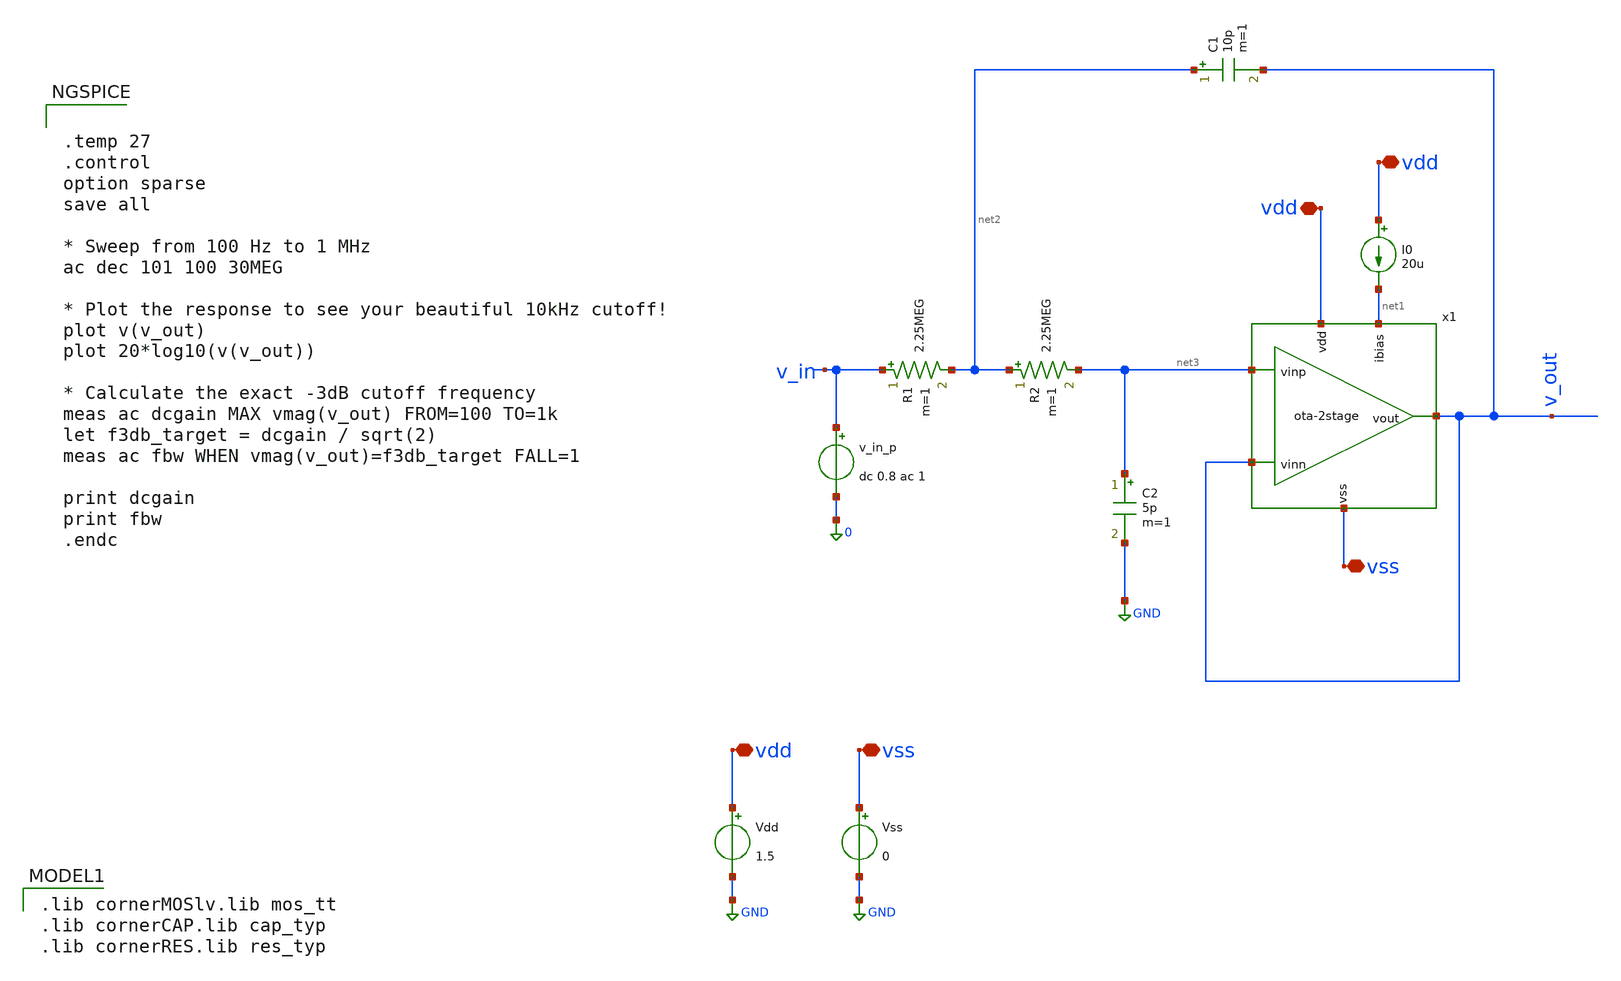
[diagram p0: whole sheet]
** sch_path: Testbench/ota-2stage_tb-sk-lpf.sch
**.subckt ota-2stage_tb-sk-lpf vdd vdd vdd vss vss
*.iopin vdd
*.iopin vdd
*.iopin vdd
*.iopin vss
*.iopin vss
I0 vdd net1 20u
Vdd vdd GND 1.5
Vss vss GND 0
v_in_p v_in 0 dc 0.8 ac 1
R1 v_in net2 2.25MEG m=1
R2 net2 net3 2.25MEG m=1
C2 net3 GND 5p m=1
C1 net2 v_out 10p m=1
x1 vdd net1 v_out v_out net3 vss ota-2stage
**** begin user architecture code


.temp 27
.control
option sparse
save all

* Sweep from 100 Hz to 1 MHz
ac dec 101 100 30MEG

* Plot the response to see your beautiful 10kHz cutoff!
plot v(v_out)
plot 20*log10(v(v_out))

* Calculate the exact -3dB cutoff frequency
meas ac dcgain MAX vmag(v_out) FROM=100 TO=1k
let f3db_target = dcgain / sqrt(2)
meas ac fbw WHEN vmag(v_out)=f3db_target FALL=1

print dcgain
print fbw
.endc


 .lib cornerMOSlv.lib mos_tt
.lib cornerCAP.lib cap_typ
.lib cornerRES.lib res_typ

**** end user architecture code
**.ends

* expanding   symbol:  ota-2stage.sym # of pins=6
** sym_path: Testbench/ota-2stage.sym
** sch_path: Testbench/ota-2stage.sch
.subckt ota-2stage vdd ibias vinn vout vinp vss
*.iopin vdd
*.iopin vss
*.ipin ibias
*.iopin vout
*.ipin vinn
*.ipin vinp
XM1 net1 vinn net3 net3 sg13_lv_nmos w=1u l=2u ng=1 m=1 mm_ok=1
XM2 net2 vinp net3 net3 sg13_lv_nmos w=1u l=2u ng=1 m=1 mm_ok=1
XM4 net2 net1 vdd vdd sg13_lv_pmos w=1u l=2u ng=1 m=1 mm_ok=1
XM3 net1 net1 vdd vdd sg13_lv_pmos w=1u l=2u ng=1 m=1 mm_ok=1
XM5 vout net2 vdd vdd sg13_lv_pmos w=9.5u l=2u ng=1 m=1 mm_ok=1
XM6 ibias ibias vss vss sg13_lv_nmos w=2u l=2u ng=1 m=1 mm_ok=1
XM7 net3 ibias vss vss sg13_lv_nmos w=0.5u l=2u ng=1 m=1 mm_ok=1
XM8 vout ibias vss vss sg13_lv_nmos w=1u l=2u ng=1 m=1 mm_ok=1
XCM vout net4 cap_cmim w=19.5e-6 l=19.5e-6 m=1 mm_ok=1
XRN net2 net4 GND rhigh w=1e-6 l=12.6e-6 m=1 b=0 mm_ok=1
.ends

.GLOBAL GND
.end
